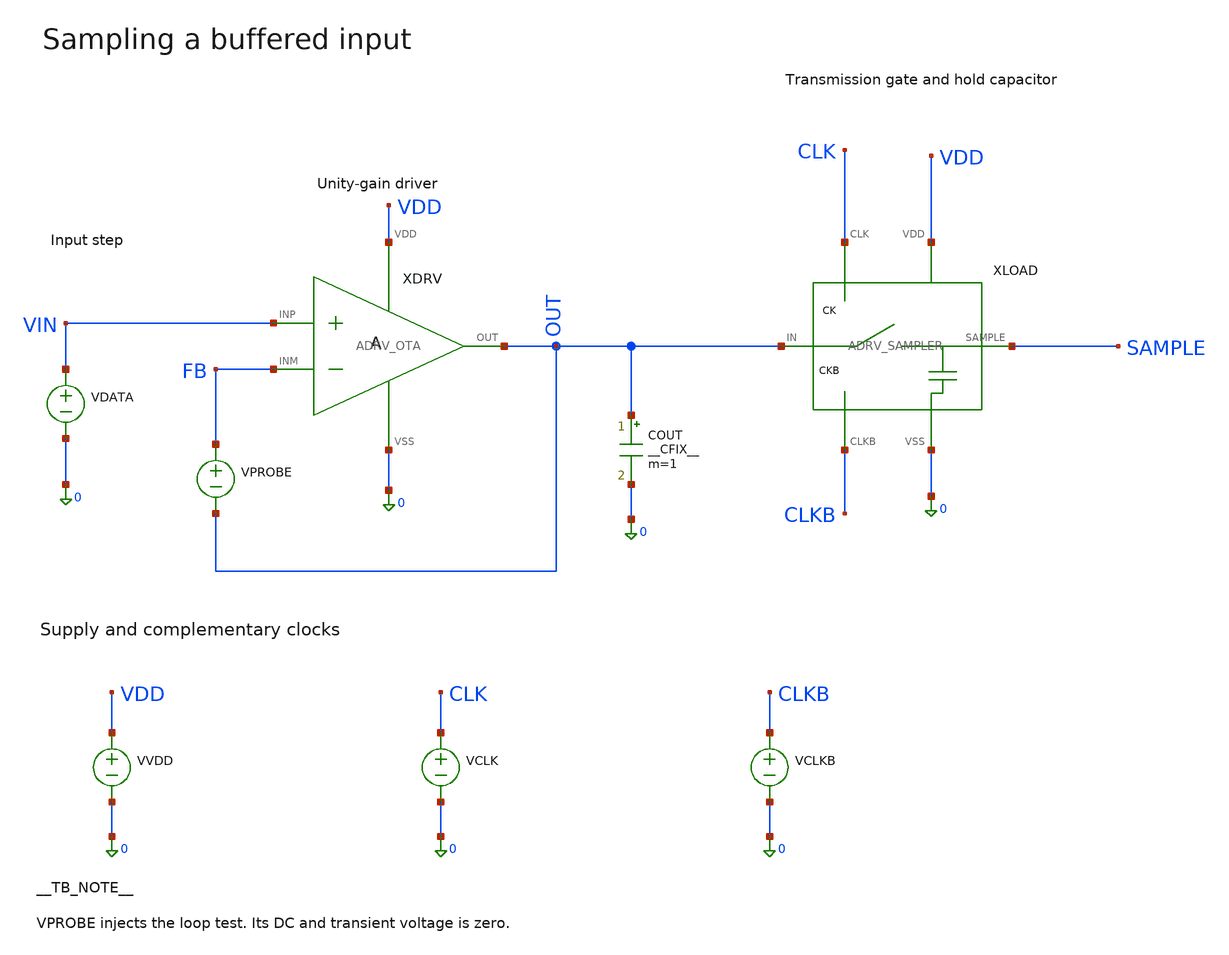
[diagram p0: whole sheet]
** sch_path: examples/sky130-adc-driver/TB_ADRV_SAMPLE.sch
**.subckt TB_ADRV_SAMPLE
XDRV VIN FB OUT VDD 0 ADRV_OTA
XLOAD OUT CLK CLKB SAMPLE VDD 0 ADRV_SAMPLER
VDATA VIN 0 __VDATA__
VPROBE FB OUT __VPROBE__
COUT OUT 0 __CFIX__ m=1
VVDD VDD 0 __VVDD__
VCLK CLK 0 __VCLK__
VCLKB CLKB 0 __VCLKB__
**.ends

* expanding   symbol:  ADRV_OTA.sym # of pins=5
** sym_path: examples/sky130-adc-driver/ADRV_OTA.sym
** sch_path: examples/sky130-adc-driver/ADRV_OTA.sch
.subckt ADRV_OTA INP INM OUT VDD VSS
*.iopin VDD
*.iopin VSS
*.ipin INP
*.ipin INM
*.opin OUT
XPREF VB VB VDD VDD sky130_fd_pr__pfet_01v8 w=1 l=1 nf=1 ad=0.3 as=0.3 pd=2.6 ps=2.6 m=1
XNREF VB VB VSS VSS sky130_fd_pr__nfet_01v8 w=1 l=1 nf=1 ad=0.3 as=0.3 pd=2.6 ps=2.6 m=1
XLA VX VX VDD VDD sky130_fd_pr__pfet_01v8 w=1 l=1 nf=1 ad=0.3 as=0.3 pd=2.6 ps=2.6 m=1
XLB OUT VX VDD VDD sky130_fd_pr__pfet_01v8 w=1 l=1 nf=1 ad=0.3 as=0.3 pd=2.6 ps=2.6 m=1
XIP VX INP TAIL VSS sky130_fd_pr__nfet_01v8 w=1 l=1 nf=1 ad=0.3 as=0.3 pd=2.6 ps=2.6 m=1
XIM OUT INM TAIL VSS sky130_fd_pr__nfet_01v8 w=1 l=1 nf=1 ad=0.3 as=0.3 pd=2.6 ps=2.6 m=1
XTAIL TAIL VB VSS VSS sky130_fd_pr__nfet_01v8 w=1 l=1 nf=1 ad=0.3 as=0.3 pd=2.6 ps=2.6 m=1
.ends


* expanding   symbol:  ADRV_SAMPLER.sym # of pins=6
** sym_path: examples/sky130-adc-driver/ADRV_SAMPLER.sym
** sch_path: examples/sky130-adc-driver/ADRV_SAMPLER.sch
.subckt ADRV_SAMPLER IN CLK CLKB SAMPLE VDD VSS
*.ipin IN
*.opin SAMPLE
*.ipin CLK
*.ipin CLKB
*.iopin VDD
*.iopin VSS
XSN SAMPLE CLK IN VSS sky130_fd_pr__nfet_01v8 w=1 l=1 nf=1 ad=0.3 as=0.3 pd=2.6 ps=2.6 m=1
XSP SAMPLE CLKB IN VDD sky130_fd_pr__pfet_01v8 w=1 l=1 nf=1 ad=0.3 as=0.3 pd=2.6 ps=2.6 m=1
CSH SAMPLE VSS __CS__ m=1
.ends

.end
